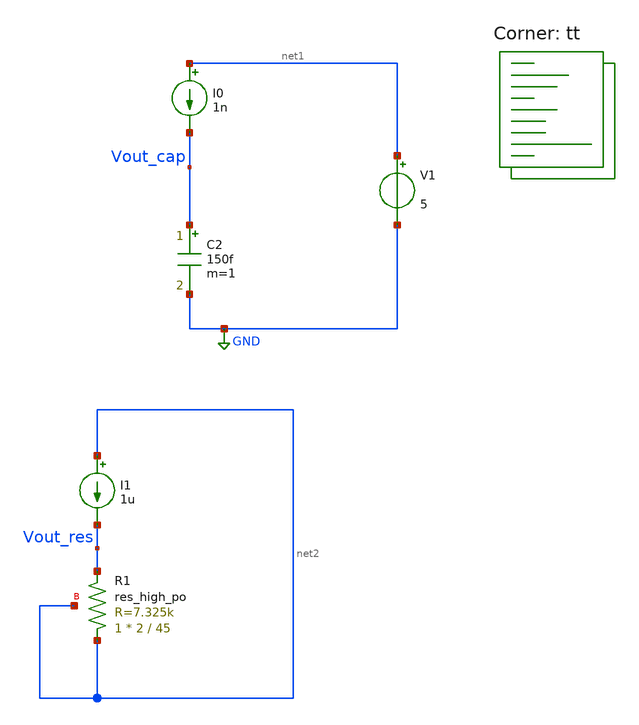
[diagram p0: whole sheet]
** sch_path: xschem/misc/testing/cap.sch
**.subckt cap
I0 net1 Vout_cap 1n
V1 net1 GND 5
C2 Vout_cap GND 150f m=1
I1 net2 Vout_res 1u
XR1 net2 Vout_res net2 sky130_fd_pr__res_high_po W=2 L=45 mult=1 m=1
**** begin user architecture code
.lib $::SKYWATER_MODELS/sky130.lib.spice tt


.param temp=27

.op
*.ac dec 10 1 1G
.dc temp -40 100 1

.control
run
plot Vout_cap
plot Vout_res

.endc

.save all



**** end user architecture code
**.ends
.GLOBAL GND
.end
